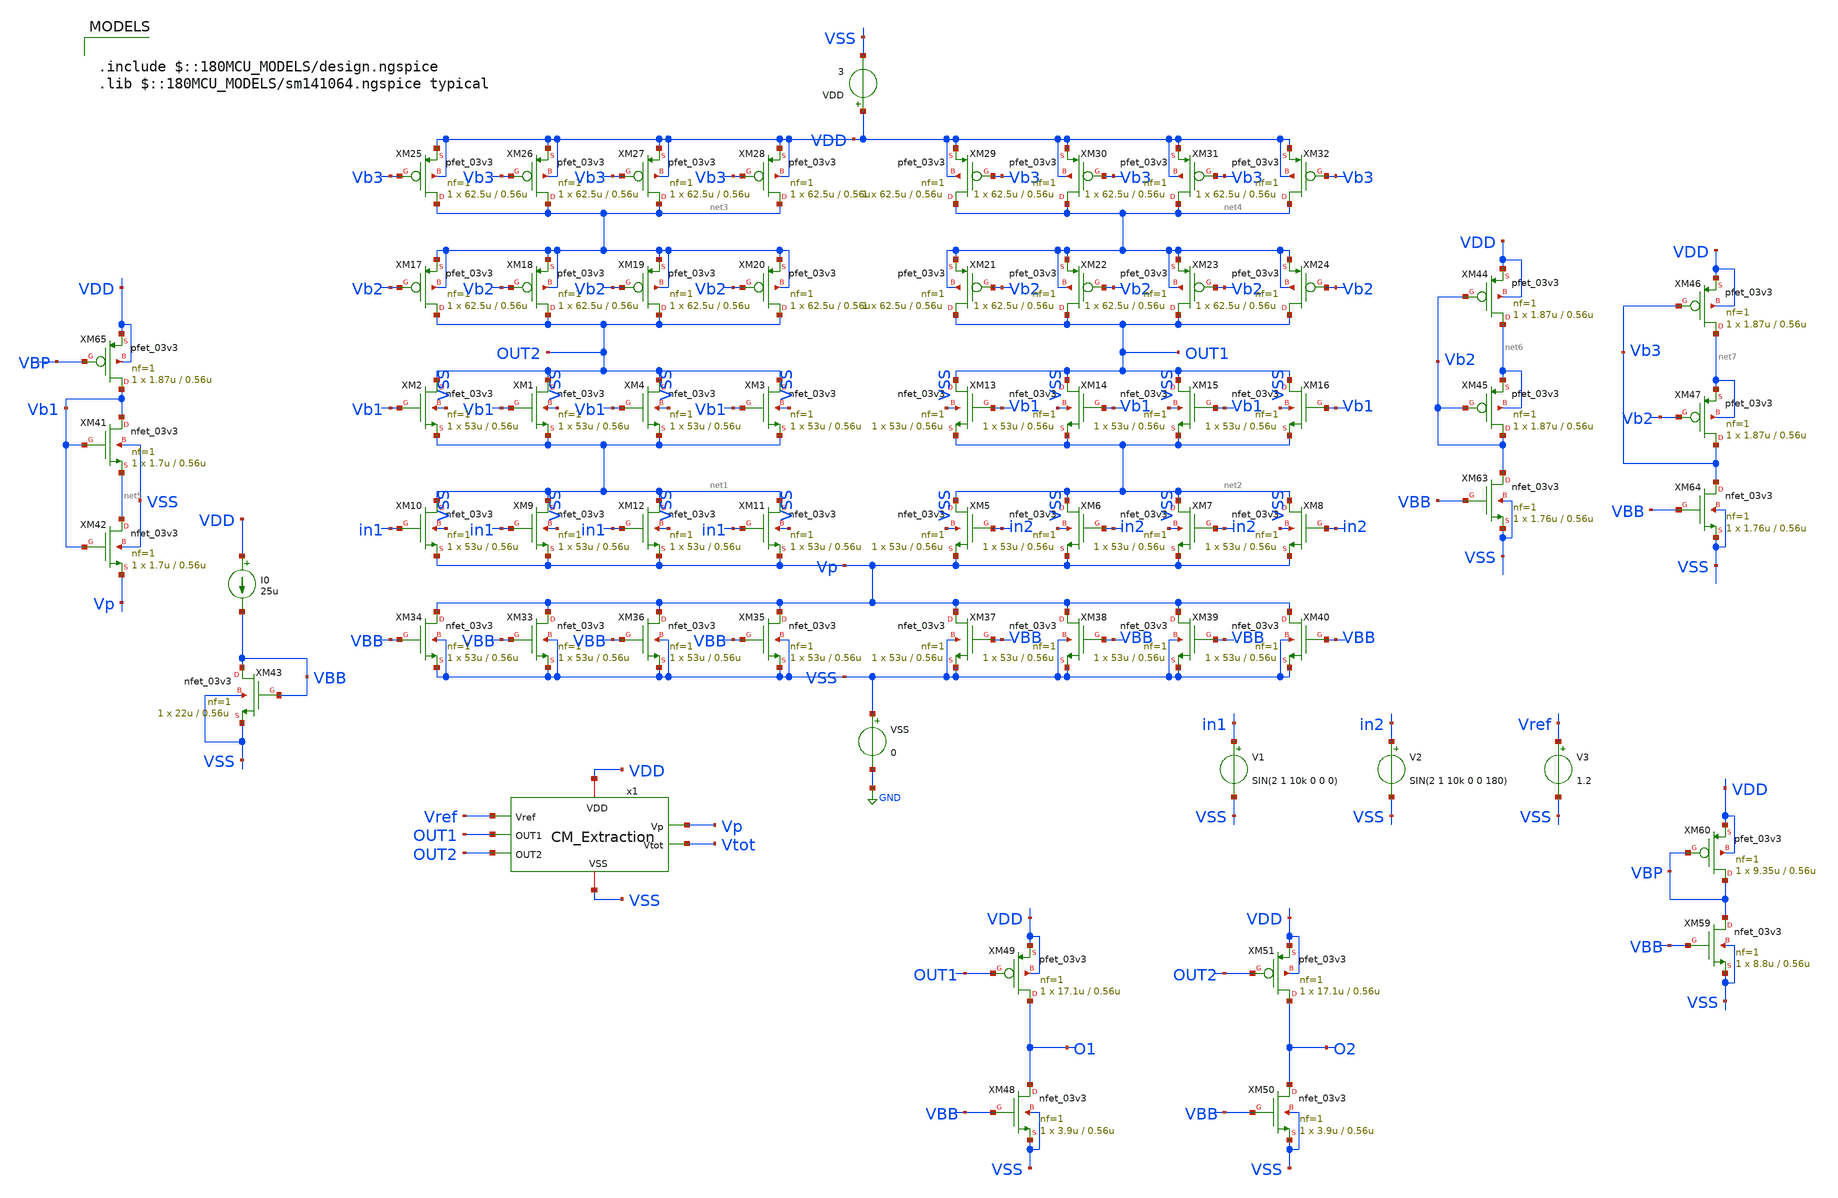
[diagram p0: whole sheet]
** sch_path: SCOP_INPUT_AND_MUX_PAKISTAN_03/Xschem/Others/Diff_Amp.sch
**.subckt Diff_Amp
XM9 net1 in1 Vp VSS nfet_03v3 L=0.56u W=53u nf=1 ad='int((nf+1)/2) * W/nf * 0.18u' as='int((nf+2)/2) * W/nf * 0.18u'
+ pd='2*int((nf+1)/2) * (W/nf + 0.18u)' ps='2*int((nf+2)/2) * (W/nf + 0.18u)' nrd='0.18u / W' nrs='0.18u / W'
+ sa=0 sb=0 sd=0 m=1
XM10 net1 in1 Vp VSS nfet_03v3 L=0.56u W=53u nf=1 ad='int((nf+1)/2) * W/nf * 0.18u' as='int((nf+2)/2) * W/nf * 0.18u'
+ pd='2*int((nf+1)/2) * (W/nf + 0.18u)' ps='2*int((nf+2)/2) * (W/nf + 0.18u)' nrd='0.18u / W' nrs='0.18u / W'
+ sa=0 sb=0 sd=0 m=1
XM11 net1 in1 Vp VSS nfet_03v3 L=0.56u W=53u nf=1 ad='int((nf+1)/2) * W/nf * 0.18u' as='int((nf+2)/2) * W/nf * 0.18u'
+ pd='2*int((nf+1)/2) * (W/nf + 0.18u)' ps='2*int((nf+2)/2) * (W/nf + 0.18u)' nrd='0.18u / W' nrs='0.18u / W'
+ sa=0 sb=0 sd=0 m=1
XM12 net1 in1 Vp VSS nfet_03v3 L=0.56u W=53u nf=1 ad='int((nf+1)/2) * W/nf * 0.18u' as='int((nf+2)/2) * W/nf * 0.18u'
+ pd='2*int((nf+1)/2) * (W/nf + 0.18u)' ps='2*int((nf+2)/2) * (W/nf + 0.18u)' nrd='0.18u / W' nrs='0.18u / W'
+ sa=0 sb=0 sd=0 m=1
XM1 OUT2 Vb1 net1 VSS nfet_03v3 L=0.56u W=53u nf=1 ad='int((nf+1)/2) * W/nf * 0.18u' as='int((nf+2)/2) * W/nf * 0.18u'
+ pd='2*int((nf+1)/2) * (W/nf + 0.18u)' ps='2*int((nf+2)/2) * (W/nf + 0.18u)' nrd='0.18u / W' nrs='0.18u / W'
+ sa=0 sb=0 sd=0 m=1
XM2 OUT2 Vb1 net1 VSS nfet_03v3 L=0.56u W=53u nf=1 ad='int((nf+1)/2) * W/nf * 0.18u' as='int((nf+2)/2) * W/nf * 0.18u'
+ pd='2*int((nf+1)/2) * (W/nf + 0.18u)' ps='2*int((nf+2)/2) * (W/nf + 0.18u)' nrd='0.18u / W' nrs='0.18u / W'
+ sa=0 sb=0 sd=0 m=1
XM3 OUT2 Vb1 net1 VSS nfet_03v3 L=0.56u W=53u nf=1 ad='int((nf+1)/2) * W/nf * 0.18u' as='int((nf+2)/2) * W/nf * 0.18u'
+ pd='2*int((nf+1)/2) * (W/nf + 0.18u)' ps='2*int((nf+2)/2) * (W/nf + 0.18u)' nrd='0.18u / W' nrs='0.18u / W'
+ sa=0 sb=0 sd=0 m=1
XM4 OUT2 Vb1 net1 VSS nfet_03v3 L=0.56u W=53u nf=1 ad='int((nf+1)/2) * W/nf * 0.18u' as='int((nf+2)/2) * W/nf * 0.18u'
+ pd='2*int((nf+1)/2) * (W/nf + 0.18u)' ps='2*int((nf+2)/2) * (W/nf + 0.18u)' nrd='0.18u / W' nrs='0.18u / W'
+ sa=0 sb=0 sd=0 m=1
XM5 net2 in2 Vp VSS nfet_03v3 L=0.56u W=53u nf=1 ad='int((nf+1)/2) * W/nf * 0.18u' as='int((nf+2)/2) * W/nf * 0.18u'
+ pd='2*int((nf+1)/2) * (W/nf + 0.18u)' ps='2*int((nf+2)/2) * (W/nf + 0.18u)' nrd='0.18u / W' nrs='0.18u / W'
+ sa=0 sb=0 sd=0 m=1
XM6 net2 in2 Vp VSS nfet_03v3 L=0.56u W=53u nf=1 ad='int((nf+1)/2) * W/nf * 0.18u' as='int((nf+2)/2) * W/nf * 0.18u'
+ pd='2*int((nf+1)/2) * (W/nf + 0.18u)' ps='2*int((nf+2)/2) * (W/nf + 0.18u)' nrd='0.18u / W' nrs='0.18u / W'
+ sa=0 sb=0 sd=0 m=1
XM7 net2 in2 Vp VSS nfet_03v3 L=0.56u W=53u nf=1 ad='int((nf+1)/2) * W/nf * 0.18u' as='int((nf+2)/2) * W/nf * 0.18u'
+ pd='2*int((nf+1)/2) * (W/nf + 0.18u)' ps='2*int((nf+2)/2) * (W/nf + 0.18u)' nrd='0.18u / W' nrs='0.18u / W'
+ sa=0 sb=0 sd=0 m=1
XM8 net2 in2 Vp VSS nfet_03v3 L=0.56u W=53u nf=1 ad='int((nf+1)/2) * W/nf * 0.18u' as='int((nf+2)/2) * W/nf * 0.18u'
+ pd='2*int((nf+1)/2) * (W/nf + 0.18u)' ps='2*int((nf+2)/2) * (W/nf + 0.18u)' nrd='0.18u / W' nrs='0.18u / W'
+ sa=0 sb=0 sd=0 m=1
XM13 OUT1 Vb1 net2 VSS nfet_03v3 L=0.56u W=53u nf=1 ad='int((nf+1)/2) * W/nf * 0.18u' as='int((nf+2)/2) * W/nf * 0.18u'
+ pd='2*int((nf+1)/2) * (W/nf + 0.18u)' ps='2*int((nf+2)/2) * (W/nf + 0.18u)' nrd='0.18u / W' nrs='0.18u / W'
+ sa=0 sb=0 sd=0 m=1
XM14 OUT1 Vb1 net2 VSS nfet_03v3 L=0.56u W=53u nf=1 ad='int((nf+1)/2) * W/nf * 0.18u' as='int((nf+2)/2) * W/nf * 0.18u'
+ pd='2*int((nf+1)/2) * (W/nf + 0.18u)' ps='2*int((nf+2)/2) * (W/nf + 0.18u)' nrd='0.18u / W' nrs='0.18u / W'
+ sa=0 sb=0 sd=0 m=1
XM15 OUT1 Vb1 net2 VSS nfet_03v3 L=0.56u W=53u nf=1 ad='int((nf+1)/2) * W/nf * 0.18u' as='int((nf+2)/2) * W/nf * 0.18u'
+ pd='2*int((nf+1)/2) * (W/nf + 0.18u)' ps='2*int((nf+2)/2) * (W/nf + 0.18u)' nrd='0.18u / W' nrs='0.18u / W'
+ sa=0 sb=0 sd=0 m=1
XM16 OUT1 Vb1 net2 VSS nfet_03v3 L=0.56u W=53u nf=1 ad='int((nf+1)/2) * W/nf * 0.18u' as='int((nf+2)/2) * W/nf * 0.18u'
+ pd='2*int((nf+1)/2) * (W/nf + 0.18u)' ps='2*int((nf+2)/2) * (W/nf + 0.18u)' nrd='0.18u / W' nrs='0.18u / W'
+ sa=0 sb=0 sd=0 m=1
XM17 OUT2 Vb2 net3 net3 pfet_03v3 L=0.56u W=62.5u nf=1 ad='int((nf+1)/2) * W/nf * 0.18u' as='int((nf+2)/2) * W/nf * 0.18u'
+ pd='2*int((nf+1)/2) * (W/nf + 0.18u)' ps='2*int((nf+2)/2) * (W/nf + 0.18u)' nrd='0.18u / W' nrs='0.18u / W'
+ sa=0 sb=0 sd=0 m=1
XM18 OUT2 Vb2 net3 net3 pfet_03v3 L=0.56u W=62.5u nf=1 ad='int((nf+1)/2) * W/nf * 0.18u' as='int((nf+2)/2) * W/nf * 0.18u'
+ pd='2*int((nf+1)/2) * (W/nf + 0.18u)' ps='2*int((nf+2)/2) * (W/nf + 0.18u)' nrd='0.18u / W' nrs='0.18u / W'
+ sa=0 sb=0 sd=0 m=1
XM19 OUT2 Vb2 net3 net3 pfet_03v3 L=0.56u W=62.5u nf=1 ad='int((nf+1)/2) * W/nf * 0.18u' as='int((nf+2)/2) * W/nf * 0.18u'
+ pd='2*int((nf+1)/2) * (W/nf + 0.18u)' ps='2*int((nf+2)/2) * (W/nf + 0.18u)' nrd='0.18u / W' nrs='0.18u / W'
+ sa=0 sb=0 sd=0 m=1
XM20 OUT2 Vb2 net3 net3 pfet_03v3 L=0.56u W=62.5u nf=1 ad='int((nf+1)/2) * W/nf * 0.18u' as='int((nf+2)/2) * W/nf * 0.18u'
+ pd='2*int((nf+1)/2) * (W/nf + 0.18u)' ps='2*int((nf+2)/2) * (W/nf + 0.18u)' nrd='0.18u / W' nrs='0.18u / W'
+ sa=0 sb=0 sd=0 m=1
XM21 OUT1 Vb2 net4 net4 pfet_03v3 L=0.56u W=62.5u nf=1 ad='int((nf+1)/2) * W/nf * 0.18u' as='int((nf+2)/2) * W/nf * 0.18u'
+ pd='2*int((nf+1)/2) * (W/nf + 0.18u)' ps='2*int((nf+2)/2) * (W/nf + 0.18u)' nrd='0.18u / W' nrs='0.18u / W'
+ sa=0 sb=0 sd=0 m=1
XM22 OUT1 Vb2 net4 net4 pfet_03v3 L=0.56u W=62.5u nf=1 ad='int((nf+1)/2) * W/nf * 0.18u' as='int((nf+2)/2) * W/nf * 0.18u'
+ pd='2*int((nf+1)/2) * (W/nf + 0.18u)' ps='2*int((nf+2)/2) * (W/nf + 0.18u)' nrd='0.18u / W' nrs='0.18u / W'
+ sa=0 sb=0 sd=0 m=1
XM23 OUT1 Vb2 net4 net4 pfet_03v3 L=0.56u W=62.5u nf=1 ad='int((nf+1)/2) * W/nf * 0.18u' as='int((nf+2)/2) * W/nf * 0.18u'
+ pd='2*int((nf+1)/2) * (W/nf + 0.18u)' ps='2*int((nf+2)/2) * (W/nf + 0.18u)' nrd='0.18u / W' nrs='0.18u / W'
+ sa=0 sb=0 sd=0 m=1
XM24 OUT1 Vb2 net4 net4 pfet_03v3 L=0.56u W=62.5u nf=1 ad='int((nf+1)/2) * W/nf * 0.18u' as='int((nf+2)/2) * W/nf * 0.18u'
+ pd='2*int((nf+1)/2) * (W/nf + 0.18u)' ps='2*int((nf+2)/2) * (W/nf + 0.18u)' nrd='0.18u / W' nrs='0.18u / W'
+ sa=0 sb=0 sd=0 m=1
XM25 net3 Vb3 VDD VDD pfet_03v3 L=0.56u W=62.5u nf=1 ad='int((nf+1)/2) * W/nf * 0.18u' as='int((nf+2)/2) * W/nf * 0.18u'
+ pd='2*int((nf+1)/2) * (W/nf + 0.18u)' ps='2*int((nf+2)/2) * (W/nf + 0.18u)' nrd='0.18u / W' nrs='0.18u / W'
+ sa=0 sb=0 sd=0 m=1
XM26 net3 Vb3 VDD VDD pfet_03v3 L=0.56u W=62.5u nf=1 ad='int((nf+1)/2) * W/nf * 0.18u' as='int((nf+2)/2) * W/nf * 0.18u'
+ pd='2*int((nf+1)/2) * (W/nf + 0.18u)' ps='2*int((nf+2)/2) * (W/nf + 0.18u)' nrd='0.18u / W' nrs='0.18u / W'
+ sa=0 sb=0 sd=0 m=1
XM27 net3 Vb3 VDD VDD pfet_03v3 L=0.56u W=62.5u nf=1 ad='int((nf+1)/2) * W/nf * 0.18u' as='int((nf+2)/2) * W/nf * 0.18u'
+ pd='2*int((nf+1)/2) * (W/nf + 0.18u)' ps='2*int((nf+2)/2) * (W/nf + 0.18u)' nrd='0.18u / W' nrs='0.18u / W'
+ sa=0 sb=0 sd=0 m=1
XM28 net3 Vb3 VDD VDD pfet_03v3 L=0.56u W=62.5u nf=1 ad='int((nf+1)/2) * W/nf * 0.18u' as='int((nf+2)/2) * W/nf * 0.18u'
+ pd='2*int((nf+1)/2) * (W/nf + 0.18u)' ps='2*int((nf+2)/2) * (W/nf + 0.18u)' nrd='0.18u / W' nrs='0.18u / W'
+ sa=0 sb=0 sd=0 m=1
XM29 net4 Vb3 VDD VDD pfet_03v3 L=0.56u W=62.5u nf=1 ad='int((nf+1)/2) * W/nf * 0.18u' as='int((nf+2)/2) * W/nf * 0.18u'
+ pd='2*int((nf+1)/2) * (W/nf + 0.18u)' ps='2*int((nf+2)/2) * (W/nf + 0.18u)' nrd='0.18u / W' nrs='0.18u / W'
+ sa=0 sb=0 sd=0 m=1
XM30 net4 Vb3 VDD VDD pfet_03v3 L=0.56u W=62.5u nf=1 ad='int((nf+1)/2) * W/nf * 0.18u' as='int((nf+2)/2) * W/nf * 0.18u'
+ pd='2*int((nf+1)/2) * (W/nf + 0.18u)' ps='2*int((nf+2)/2) * (W/nf + 0.18u)' nrd='0.18u / W' nrs='0.18u / W'
+ sa=0 sb=0 sd=0 m=1
XM31 net4 Vb3 VDD VDD pfet_03v3 L=0.56u W=62.5u nf=1 ad='int((nf+1)/2) * W/nf * 0.18u' as='int((nf+2)/2) * W/nf * 0.18u'
+ pd='2*int((nf+1)/2) * (W/nf + 0.18u)' ps='2*int((nf+2)/2) * (W/nf + 0.18u)' nrd='0.18u / W' nrs='0.18u / W'
+ sa=0 sb=0 sd=0 m=1
XM32 net4 Vb3 VDD VDD pfet_03v3 L=0.56u W=62.5u nf=1 ad='int((nf+1)/2) * W/nf * 0.18u' as='int((nf+2)/2) * W/nf * 0.18u'
+ pd='2*int((nf+1)/2) * (W/nf + 0.18u)' ps='2*int((nf+2)/2) * (W/nf + 0.18u)' nrd='0.18u / W' nrs='0.18u / W'
+ sa=0 sb=0 sd=0 m=1
XM33 Vp VBB VSS VSS nfet_03v3 L=0.56u W=53u nf=1 ad='int((nf+1)/2) * W/nf * 0.18u' as='int((nf+2)/2) * W/nf * 0.18u'
+ pd='2*int((nf+1)/2) * (W/nf + 0.18u)' ps='2*int((nf+2)/2) * (W/nf + 0.18u)' nrd='0.18u / W' nrs='0.18u / W'
+ sa=0 sb=0 sd=0 m=1
XM34 Vp VBB VSS VSS nfet_03v3 L=0.56u W=53u nf=1 ad='int((nf+1)/2) * W/nf * 0.18u' as='int((nf+2)/2) * W/nf * 0.18u'
+ pd='2*int((nf+1)/2) * (W/nf + 0.18u)' ps='2*int((nf+2)/2) * (W/nf + 0.18u)' nrd='0.18u / W' nrs='0.18u / W'
+ sa=0 sb=0 sd=0 m=1
XM35 Vp VBB VSS VSS nfet_03v3 L=0.56u W=53u nf=1 ad='int((nf+1)/2) * W/nf * 0.18u' as='int((nf+2)/2) * W/nf * 0.18u'
+ pd='2*int((nf+1)/2) * (W/nf + 0.18u)' ps='2*int((nf+2)/2) * (W/nf + 0.18u)' nrd='0.18u / W' nrs='0.18u / W'
+ sa=0 sb=0 sd=0 m=1
XM36 Vp VBB VSS VSS nfet_03v3 L=0.56u W=53u nf=1 ad='int((nf+1)/2) * W/nf * 0.18u' as='int((nf+2)/2) * W/nf * 0.18u'
+ pd='2*int((nf+1)/2) * (W/nf + 0.18u)' ps='2*int((nf+2)/2) * (W/nf + 0.18u)' nrd='0.18u / W' nrs='0.18u / W'
+ sa=0 sb=0 sd=0 m=1
XM37 Vp VBB VSS VSS nfet_03v3 L=0.56u W=53u nf=1 ad='int((nf+1)/2) * W/nf * 0.18u' as='int((nf+2)/2) * W/nf * 0.18u'
+ pd='2*int((nf+1)/2) * (W/nf + 0.18u)' ps='2*int((nf+2)/2) * (W/nf + 0.18u)' nrd='0.18u / W' nrs='0.18u / W'
+ sa=0 sb=0 sd=0 m=1
XM38 Vp VBB VSS VSS nfet_03v3 L=0.56u W=53u nf=1 ad='int((nf+1)/2) * W/nf * 0.18u' as='int((nf+2)/2) * W/nf * 0.18u'
+ pd='2*int((nf+1)/2) * (W/nf + 0.18u)' ps='2*int((nf+2)/2) * (W/nf + 0.18u)' nrd='0.18u / W' nrs='0.18u / W'
+ sa=0 sb=0 sd=0 m=1
XM39 Vp VBB VSS VSS nfet_03v3 L=0.56u W=53u nf=1 ad='int((nf+1)/2) * W/nf * 0.18u' as='int((nf+2)/2) * W/nf * 0.18u'
+ pd='2*int((nf+1)/2) * (W/nf + 0.18u)' ps='2*int((nf+2)/2) * (W/nf + 0.18u)' nrd='0.18u / W' nrs='0.18u / W'
+ sa=0 sb=0 sd=0 m=1
XM40 Vp VBB VSS VSS nfet_03v3 L=0.56u W=53u nf=1 ad='int((nf+1)/2) * W/nf * 0.18u' as='int((nf+2)/2) * W/nf * 0.18u'
+ pd='2*int((nf+1)/2) * (W/nf + 0.18u)' ps='2*int((nf+2)/2) * (W/nf + 0.18u)' nrd='0.18u / W' nrs='0.18u / W'
+ sa=0 sb=0 sd=0 m=1
XM43 VBB VBB VSS VSS nfet_03v3 L=0.56u W=22u nf=1 ad='int((nf+1)/2) * W/nf * 0.18u' as='int((nf+2)/2) * W/nf * 0.18u'
+ pd='2*int((nf+1)/2) * (W/nf + 0.18u)' ps='2*int((nf+2)/2) * (W/nf + 0.18u)' nrd='0.18u / W' nrs='0.18u / W'
+ sa=0 sb=0 sd=0 m=1
I0 VDD VBB 25u
VSS VSS GND 0
VDD VDD VSS 3
XM41 Vb1 Vb1 net5 VSS nfet_03v3 L=0.56u W=1.7u nf=1 ad='int((nf+1)/2) * W/nf * 0.18u' as='int((nf+2)/2) * W/nf * 0.18u'
+ pd='2*int((nf+1)/2) * (W/nf + 0.18u)' ps='2*int((nf+2)/2) * (W/nf + 0.18u)' nrd='0.18u / W' nrs='0.18u / W'
+ sa=0 sb=0 sd=0 m=1
XM42 net5 Vb1 Vp VSS nfet_03v3 L=0.56u W=1.7u nf=1 ad='int((nf+1)/2) * W/nf * 0.18u' as='int((nf+2)/2) * W/nf * 0.18u'
+ pd='2*int((nf+1)/2) * (W/nf + 0.18u)' ps='2*int((nf+2)/2) * (W/nf + 0.18u)' nrd='0.18u / W' nrs='0.18u / W'
+ sa=0 sb=0 sd=0 m=1
XM44 net6 Vb2 VDD VDD pfet_03v3 L=0.56u W=1.87u nf=1 ad='int((nf+1)/2) * W/nf * 0.18u' as='int((nf+2)/2) * W/nf * 0.18u'
+ pd='2*int((nf+1)/2) * (W/nf + 0.18u)' ps='2*int((nf+2)/2) * (W/nf + 0.18u)' nrd='0.18u / W' nrs='0.18u / W'
+ sa=0 sb=0 sd=0 m=1
XM45 Vb2 Vb2 net6 net6 pfet_03v3 L=0.56u W=1.87u nf=1 ad='int((nf+1)/2) * W/nf * 0.18u' as='int((nf+2)/2) * W/nf * 0.18u'
+ pd='2*int((nf+1)/2) * (W/nf + 0.18u)' ps='2*int((nf+2)/2) * (W/nf + 0.18u)' nrd='0.18u / W' nrs='0.18u / W'
+ sa=0 sb=0 sd=0 m=1
XM46 net7 Vb3 VDD VDD pfet_03v3 L=0.56u W=1.87u nf=1 ad='int((nf+1)/2) * W/nf * 0.18u' as='int((nf+2)/2) * W/nf * 0.18u'
+ pd='2*int((nf+1)/2) * (W/nf + 0.18u)' ps='2*int((nf+2)/2) * (W/nf + 0.18u)' nrd='0.18u / W' nrs='0.18u / W'
+ sa=0 sb=0 sd=0 m=1
XM47 Vb3 Vb2 net7 net7 pfet_03v3 L=0.56u W=1.87u nf=1 ad='int((nf+1)/2) * W/nf * 0.18u' as='int((nf+2)/2) * W/nf * 0.18u'
+ pd='2*int((nf+1)/2) * (W/nf + 0.18u)' ps='2*int((nf+2)/2) * (W/nf + 0.18u)' nrd='0.18u / W' nrs='0.18u / W'
+ sa=0 sb=0 sd=0 m=1
V1 in1 VSS SIN(2 1 10k 0 0 0)
V2 in2 VSS SIN(2 1 10k 0 0 180)
V3 Vref VSS 1.2
XM59 VBP VBB VSS VSS nfet_03v3 L=0.56u W=8.8u nf=1 ad='int((nf+1)/2) * W/nf * 0.18u' as='int((nf+2)/2) * W/nf * 0.18u'
+ pd='2*int((nf+1)/2) * (W/nf + 0.18u)' ps='2*int((nf+2)/2) * (W/nf + 0.18u)' nrd='0.18u / W' nrs='0.18u / W'
+ sa=0 sb=0 sd=0 m=1
XM60 VBP VBP VDD VDD pfet_03v3 L=0.56u W=9.35u nf=1 ad='int((nf+1)/2) * W/nf * 0.18u' as='int((nf+2)/2) * W/nf * 0.18u'
+ pd='2*int((nf+1)/2) * (W/nf + 0.18u)' ps='2*int((nf+2)/2) * (W/nf + 0.18u)' nrd='0.18u / W' nrs='0.18u / W'
+ sa=0 sb=0 sd=0 m=1
XM63 Vb2 VBB VSS VSS nfet_03v3 L=0.56u W=1.76u nf=1 ad='int((nf+1)/2) * W/nf * 0.18u' as='int((nf+2)/2) * W/nf * 0.18u'
+ pd='2*int((nf+1)/2) * (W/nf + 0.18u)' ps='2*int((nf+2)/2) * (W/nf + 0.18u)' nrd='0.18u / W' nrs='0.18u / W'
+ sa=0 sb=0 sd=0 m=1
XM64 Vb3 VBB VSS VSS nfet_03v3 L=0.56u W=1.76u nf=1 ad='int((nf+1)/2) * W/nf * 0.18u' as='int((nf+2)/2) * W/nf * 0.18u'
+ pd='2*int((nf+1)/2) * (W/nf + 0.18u)' ps='2*int((nf+2)/2) * (W/nf + 0.18u)' nrd='0.18u / W' nrs='0.18u / W'
+ sa=0 sb=0 sd=0 m=1
XM65 Vb1 VBP VDD VDD pfet_03v3 L=0.56u W=1.87u nf=1 ad='int((nf+1)/2) * W/nf * 0.18u' as='int((nf+2)/2) * W/nf * 0.18u'
+ pd='2*int((nf+1)/2) * (W/nf + 0.18u)' ps='2*int((nf+2)/2) * (W/nf + 0.18u)' nrd='0.18u / W' nrs='0.18u / W'
+ sa=0 sb=0 sd=0 m=1
x1 Vref Vp Vtot VDD OUT1 VSS OUT2 CM_Extraction
XM48 O1 VBB VSS VSS nfet_03v3 L=0.56u W=3.9u nf=1 ad='int((nf+1)/2) * W/nf * 0.18u' as='int((nf+2)/2) * W/nf * 0.18u'
+ pd='2*int((nf+1)/2) * (W/nf + 0.18u)' ps='2*int((nf+2)/2) * (W/nf + 0.18u)' nrd='0.18u / W' nrs='0.18u / W'
+ sa=0 sb=0 sd=0 m=1
XM49 O1 OUT1 VDD VDD pfet_03v3 L=0.56u W=17.1u nf=1 ad='int((nf+1)/2) * W/nf * 0.18u' as='int((nf+2)/2) * W/nf * 0.18u'
+ pd='2*int((nf+1)/2) * (W/nf + 0.18u)' ps='2*int((nf+2)/2) * (W/nf + 0.18u)' nrd='0.18u / W' nrs='0.18u / W'
+ sa=0 sb=0 sd=0 m=1
XM50 O2 VBB VSS VSS nfet_03v3 L=0.56u W=3.9u nf=1 ad='int((nf+1)/2) * W/nf * 0.18u' as='int((nf+2)/2) * W/nf * 0.18u'
+ pd='2*int((nf+1)/2) * (W/nf + 0.18u)' ps='2*int((nf+2)/2) * (W/nf + 0.18u)' nrd='0.18u / W' nrs='0.18u / W'
+ sa=0 sb=0 sd=0 m=1
XM51 O2 OUT2 VDD VDD pfet_03v3 L=0.56u W=17.1u nf=1 ad='int((nf+1)/2) * W/nf * 0.18u' as='int((nf+2)/2) * W/nf * 0.18u'
+ pd='2*int((nf+1)/2) * (W/nf + 0.18u)' ps='2*int((nf+2)/2) * (W/nf + 0.18u)' nrd='0.18u / W' nrs='0.18u / W'
+ sa=0 sb=0 sd=0 m=1
**** begin user architecture code

.include $::180MCU_MODELS/design.ngspice
.lib $::180MCU_MODELS/sm141064.ngspice typical




.control
save all
*save all @m.xm1.m0[vdsat] @m.xm2.m0[vdsat] @m.xm1.m0[vds] @m.xm2.m0[vds]
*save all @m.xm3.m0[vdsat] @m.xm4.m0[vdsat] @m.xm3.m0[vds] @m.xm4.m0[vds]
*save all @m.xm5.m0[vdsat] @m.xm6.m0[vdsat] @m.xm5.m0[vds] @m.xm6.m0[vds]
*save all @m.xm7.m0[vdsat] @m.xm8.m0[vdsat] @m.xm7.m0[vds] @m.xm8.m0[vds]
*save all @m.xm9.m0[vdsat] @m.xm9.m0[vdsat] @m.xm12.m0[vds] @m.xm12.m0[vds]
*save all @m.xm1.m0[id] @m.xm2.m0[id] @m.xm3.m0[id] @m.xm4.m0[id]
save all @m.xm43.m0[id] @m.xm10.m0[id] @m.xm11.m0[id] @m.xm12.m0[id]
save all @m.xm34.m0[vdsat] @m.xm11.m0[vdsat] @m.xm34.m0[vds] @m.xm11.m0[vds]
dc V2 1.8 2.2 1m
*ac dec 50 1 100e9
let tf = OUT1/IN1
let gain = db(tf)
let phase = (180/pi)*ph(tf)
*plot gain
*plot phase
let id1 = @m.xm43.m0[id]
*let id2 = @m.xm2.m0[id]
*let id3 = @m.xm3.m0[id]
*let id4 = @m.xm4.m0[id]
plot id1
*let id9 = @m.xm9.m0[id]
*let id12 = @m.xm12.m0[id]
*plot id9 id10 id11 id12
*let Vov1 = @m.xm1.m0[vdsat]
*let Vds1 = @m.xm1.m0[vds]
*let Vov2 = @m.xm2.m0[vdsat]
*let Vds2 = @m.xm2.m0[vds]
*plot Vov1 Vov2 Vds1 Vds2
*let Vov3 = @m.xm3.m0[vdsat]
*let Vov4 = @m.xm4.m0[vdsat]
*let Vds3 = @m.xm3.m0[vds]
*let Vds4 = @m.xm4.m0[vds]
*plot Vov3 Vov4 Vds3 Vds4
*let Vov5 = @m.xm5.m0[vdsat]
*let Vov6 = @m.xm6.m0[vdsat]
*let Vds5 = @m.xm5.m0[vds]
*let Vds6 = @m.xm6.m0[vds]
*plot Vov5 Vov6 Vds5 Vds6
*let Vov7 = @m.xm7.m0[vdsat]
*let Vov8 = @m.xm8.m0[vdsat]
*let Vds7 = @m.xm7.m0[vds]
*let Vds8 = @m.xm8.m0[vds]
*plot Vov7 Vov8 Vds7 Vds8
*let Vov9 = @m.xm9.m0[vdsat]
*let Vds9 = @m.xm9.m0[vds]
*let Vov12 = @m.xm12.m0[vdsat]
*let Vds12 = @m.xm12.m0[vds]
*plot Vov9 Vov12 Vds9 Vds12
let Vov34 = @m.xm34.m0[vdsat]
let Vds34 = @m.xm34.m0[vds]
*let Vov11 = @m.xm11.m0[vdsat]
*let Vds11 = @m.xm11.m0[vds]
*plot Vov34 Vds34
*let gds = @m.xm1.m0[gds]
*plot v(Vp) v(Vb1) v(Vb2) v(Vb3)
*plot gds
plot v(OUT1) v(OUT2) v(Vtot)
plot v(O1) v(O2)
*plot i(VDD)
*write test_nfet_03v3.raw
.endc


**** end user architecture code
**.ends

* expanding   symbol:  Tapeout/CM_Extraction.sym # of pins=7
** sym_path: SCOP_INPUT_AND_MUX_PAKISTAN_03/Xschem/Others/CM_Extraction.sym
** sch_path: SCOP_INPUT_AND_MUX_PAKISTAN_03/Xschem/Others/CM_Extraction.sch
.subckt CM_Extraction Vref Vp Vtot VDD OUT1 VSS OUT2
*.ipin Vref
*.ipin OUT1
*.ipin OUT2
*.opin Vp
*.iopin VDD
*.iopin VSS
*.opin Vtot
R2 Vtot VB 100k m=1
R1 Vtot VA 100k m=1
R4 VD Vtot 100k m=1
R3 VC Vtot 100k m=1
XM50 VSS OUT2 VC VC pfet_03v3 L=0.56u W=9.35u nf=1 ad='int((nf+1)/2) * W/nf * 0.18u' as='int((nf+2)/2) * W/nf * 0.18u'
+ pd='2*int((nf+1)/2) * (W/nf + 0.18u)' ps='2*int((nf+2)/2) * (W/nf + 0.18u)' nrd='0.18u / W' nrs='0.18u / W'
+ sa=0 sb=0 sd=0 m=1
XM51 VSS OUT1 VD VD pfet_03v3 L=0.56u W=9.35u nf=1 ad='int((nf+1)/2) * W/nf * 0.18u' as='int((nf+2)/2) * W/nf * 0.18u'
+ pd='2*int((nf+1)/2) * (W/nf + 0.18u)' ps='2*int((nf+2)/2) * (W/nf + 0.18u)' nrd='0.18u / W' nrs='0.18u / W'
+ sa=0 sb=0 sd=0 m=1
XM61 VD VBP VDD VDD pfet_03v3 L=0.56u W=9.35u nf=1 ad='int((nf+1)/2) * W/nf * 0.18u' as='int((nf+2)/2) * W/nf * 0.18u'
+ pd='2*int((nf+1)/2) * (W/nf + 0.18u)' ps='2*int((nf+2)/2) * (W/nf + 0.18u)' nrd='0.18u / W' nrs='0.18u / W'
+ sa=0 sb=0 sd=0 m=1
XM62 VC VBP VDD VDD pfet_03v3 L=0.56u W=9.35u nf=1 ad='int((nf+1)/2) * W/nf * 0.18u' as='int((nf+2)/2) * W/nf * 0.18u'
+ pd='2*int((nf+1)/2) * (W/nf + 0.18u)' ps='2*int((nf+2)/2) * (W/nf + 0.18u)' nrd='0.18u / W' nrs='0.18u / W'
+ sa=0 sb=0 sd=0 m=1
XM59 VBP VBB VSS VSS nfet_03v3 L=0.56u W=8.8u nf=1 ad='int((nf+1)/2) * W/nf * 0.18u' as='int((nf+2)/2) * W/nf * 0.18u'
+ pd='2*int((nf+1)/2) * (W/nf + 0.18u)' ps='2*int((nf+2)/2) * (W/nf + 0.18u)' nrd='0.18u / W' nrs='0.18u / W'
+ sa=0 sb=0 sd=0 m=1
XM60 VBP VBP VDD VDD pfet_03v3 L=0.56u W=9.35u nf=1 ad='int((nf+1)/2) * W/nf * 0.18u' as='int((nf+2)/2) * W/nf * 0.18u'
+ pd='2*int((nf+1)/2) * (W/nf + 0.18u)' ps='2*int((nf+2)/2) * (W/nf + 0.18u)' nrd='0.18u / W' nrs='0.18u / W'
+ sa=0 sb=0 sd=0 m=1
XM49 VDD OUT1 VB VSS nfet_03v3 L=0.56u W=8.8u nf=1 ad='int((nf+1)/2) * W/nf * 0.18u' as='int((nf+2)/2) * W/nf * 0.18u'
+ pd='2*int((nf+1)/2) * (W/nf + 0.18u)' ps='2*int((nf+2)/2) * (W/nf + 0.18u)' nrd='0.18u / W' nrs='0.18u / W'
+ sa=0 sb=0 sd=0 m=1
XM58 VB VBB VSS VSS nfet_03v3 L=0.56u W=8.8u nf=1 ad='int((nf+1)/2) * W/nf * 0.18u' as='int((nf+2)/2) * W/nf * 0.18u'
+ pd='2*int((nf+1)/2) * (W/nf + 0.18u)' ps='2*int((nf+2)/2) * (W/nf + 0.18u)' nrd='0.18u / W' nrs='0.18u / W'
+ sa=0 sb=0 sd=0 m=1
XM48 VDD OUT2 VA VSS nfet_03v3 L=0.56u W=8.8u nf=1 ad='int((nf+1)/2) * W/nf * 0.18u' as='int((nf+2)/2) * W/nf * 0.18u'
+ pd='2*int((nf+1)/2) * (W/nf + 0.18u)' ps='2*int((nf+2)/2) * (W/nf + 0.18u)' nrd='0.18u / W' nrs='0.18u / W'
+ sa=0 sb=0 sd=0 m=1
XM57 VA VBB VSS VSS nfet_03v3 L=0.56u W=8.8u nf=1 ad='int((nf+1)/2) * W/nf * 0.18u' as='int((nf+2)/2) * W/nf * 0.18u'
+ pd='2*int((nf+1)/2) * (W/nf + 0.18u)' ps='2*int((nf+2)/2) * (W/nf + 0.18u)' nrd='0.18u / W' nrs='0.18u / W'
+ sa=0 sb=0 sd=0 m=1
XM52 net2 net1 VSS VSS nfet_03v3 L=0.56u W=21.2u nf=1 ad='int((nf+1)/2) * W/nf * 0.18u' as='int((nf+2)/2) * W/nf * 0.18u'
+ pd='2*int((nf+1)/2) * (W/nf + 0.18u)' ps='2*int((nf+2)/2) * (W/nf + 0.18u)' nrd='0.18u / W' nrs='0.18u / W'
+ sa=0 sb=0 sd=0 m=1
XM53 net1 net1 VSS VSS nfet_03v3 L=0.56u W=21.2u nf=1 ad='int((nf+1)/2) * W/nf * 0.18u' as='int((nf+2)/2) * W/nf * 0.18u'
+ pd='2*int((nf+1)/2) * (W/nf + 0.18u)' ps='2*int((nf+2)/2) * (W/nf + 0.18u)' nrd='0.18u / W' nrs='0.18u / W'
+ sa=0 sb=0 sd=0 m=1
XM54 net1 Vtot net3 net3 pfet_03v3 L=0.56u W=23.4u nf=1 ad='int((nf+1)/2) * W/nf * 0.18u' as='int((nf+2)/2) * W/nf * 0.18u'
+ pd='2*int((nf+1)/2) * (W/nf + 0.18u)' ps='2*int((nf+2)/2) * (W/nf + 0.18u)' nrd='0.18u / W' nrs='0.18u / W'
+ sa=0 sb=0 sd=0 m=1
XM55 net2 Vref net3 net3 pfet_03v3 L=0.56u W=23.4u nf=1 ad='int((nf+1)/2) * W/nf * 0.18u' as='int((nf+2)/2) * W/nf * 0.18u'
+ pd='2*int((nf+1)/2) * (W/nf + 0.18u)' ps='2*int((nf+2)/2) * (W/nf + 0.18u)' nrd='0.18u / W' nrs='0.18u / W'
+ sa=0 sb=0 sd=0 m=1
XM56 Vp net2 VSS VSS nfet_03v3 L=0.56u W=21.2u nf=1 ad='int((nf+1)/2) * W/nf * 0.18u' as='int((nf+2)/2) * W/nf * 0.18u'
+ pd='2*int((nf+1)/2) * (W/nf + 0.18u)' ps='2*int((nf+2)/2) * (W/nf + 0.18u)' nrd='0.18u / W' nrs='0.18u / W'
+ sa=0 sb=0 sd=0 m=1
XM66 net3 VBP VDD VDD pfet_03v3 L=0.56u W=23.4u nf=1 ad='int((nf+1)/2) * W/nf * 0.18u' as='int((nf+2)/2) * W/nf * 0.18u'
+ pd='2*int((nf+1)/2) * (W/nf + 0.18u)' ps='2*int((nf+2)/2) * (W/nf + 0.18u)' nrd='0.18u / W' nrs='0.18u / W'
+ sa=0 sb=0 sd=0 m=1
XM43 VBB VBB VSS VSS nfet_03v3 L=0.56u W=22u nf=1 ad='int((nf+1)/2) * W/nf * 0.18u' as='int((nf+2)/2) * W/nf * 0.18u'
+ pd='2*int((nf+1)/2) * (W/nf + 0.18u)' ps='2*int((nf+2)/2) * (W/nf + 0.18u)' nrd='0.18u / W' nrs='0.18u / W'
+ sa=0 sb=0 sd=0 m=1
I0 VDD VBB 25u
.ends

.GLOBAL GND
.end
